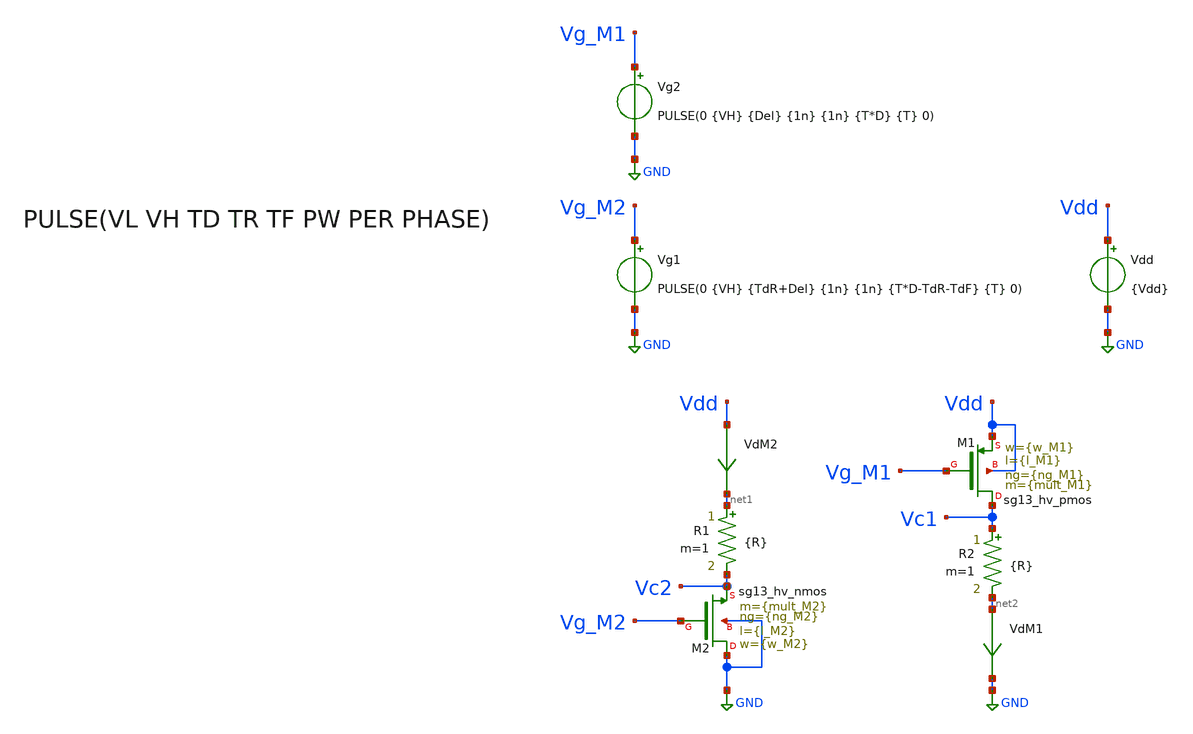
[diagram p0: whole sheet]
** sch_path: xschem/TB_hvMOS_switch_test.sch
**.subckt TB_hvMOS_switch_test
XM2 GND Vg_M2 Vc2 GND sg13_hv_nmos w={w_M2} l={l_M2} ng={ng_M2} m={mult_M2} mm_ok=1
XM1 Vc1 Vg_M1 Vdd Vdd sg13_hv_pmos w={w_M1} l={l_M1} ng={ng_M1} m={mult_M1} mm_ok=1
Vdd Vdd GND {Vdd}
VdM2 Vdd net1 0
.save i(vdm2)
VdM1 net2 GND 0
.save i(vdm1)
Vg1 Vg_M2 GND PULSE(0 {VH} {TdR+Del} {1n} {1n} {T*D-TdR-TdF} {T} 0)
Vg2 Vg_M1 GND PULSE(0 {VH} {Del} {1n} {1n} {T*D} {T} 0)
R1 net1 Vc2 {R} m=1
R2 Vc1 net2 {R} m=1
**** begin user architecture code

.lib cornerMOShv.lib mos_tt



.param Vdd = 3.3
.param R = 1.4

.param VH = 3.3
.param D = 0.5
.param T = 1u
.param TR = 7n
.param TF = 7n
.param TdR = 0.1u
.param TdF = 0.1u
.param Del = 0.25u
.param temp = 27






.save all
.control
reset
set color0 = white
tran 1n 1u
let VsdM1 = v(Vdd) - v(Vc1)
let VdsM2 = v(Vc2)
plot i(VdM1) i(VdM2)
plot v(Vc1) v(Vc2)
plot v(Vg_M1) v(Vg_M2)
plot VsdM1 VdsM2
meas TRAN td_off_M1 TRIG v(Vg_M1) VAL=0.33 RISE=1 TARG VsdM1 VAL=0.33 RISE=1
meas TRAN td_on_M1 TRIG v(Vg_M1) VAL=2.97 FALL=1 TARG VsdM1 VAL=2.97 FALL=1
meas TRAN td_on_M2 TRIG v(Vg_M2) VAL=0.33 RISE=1 TARG VdsM2 VAL=2.97 FALL=1
meas TRAN td_off_M2 TRIG v(Vg_M2) VAL=2.97 FALL=1 TARG VdsM2 VAL=0.33 RISE=1
let TdR = td_off_M1 - td_on_M2
let TdF = td_on_M1 - td_off_M2
print TdR TdF
.endc

.end




.param temp=27
.param mult_M1 = 2400
.param w_M1 =10u
*.param l_M1 = 0.2u ** Posee mayor capacidad de corriente, pero en sub-umbral conduce mucha
*+ corriente
.param l_M1 = 0.22u
.param ng_M1 = 1

.param mult_M2 = 1200
.param w_M2 =10u
.param l_M2 =0.25u
.param ng_M2 =1





**** end user architecture code
**.ends
.GLOBAL GND
.end
